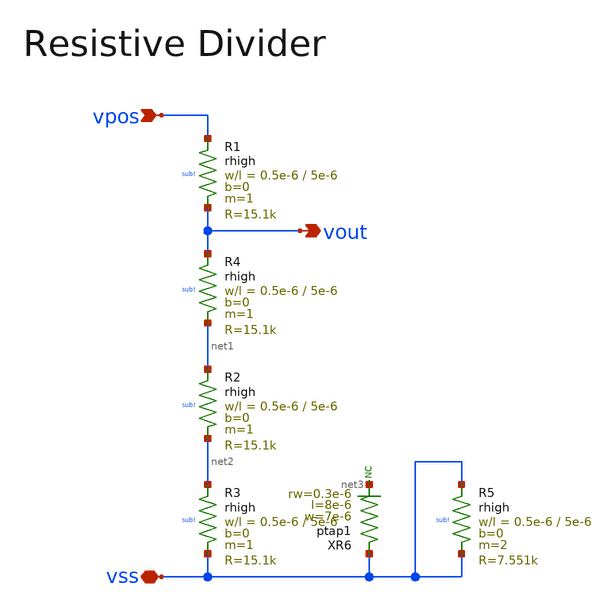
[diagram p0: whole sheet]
** sch_path: dcic_script_resistive_divider.sch
**.subckt dcic_script_resistive_divider vpos vout vss
*.ipin vpos
*.opin vout
*.iopin vss
XR1 vpos vout sub! rhigh w=0.5e-6 l=5e-6 m=1 b=0 mm_ok=1
XR2 net1 net2 sub! rhigh w=0.5e-6 l=5e-6 m=1 b=0 mm_ok=1
XR3 net2 vss sub! rhigh w=0.5e-6 l=5e-6 m=1 b=0 mm_ok=1
XR4 vout net1 sub! rhigh w=0.5e-6 l=5e-6 m=1 b=0 mm_ok=1
XR5 vss vss sub! rhigh w=0.5e-6 l=5e-6 m=2 b=0 mm_ok=1
XR6 vss net3 ptap1 R=7.913 w=7e-6 l=8e-6 rw=0.3e-6
* noconn #net3
**.ends
.end
